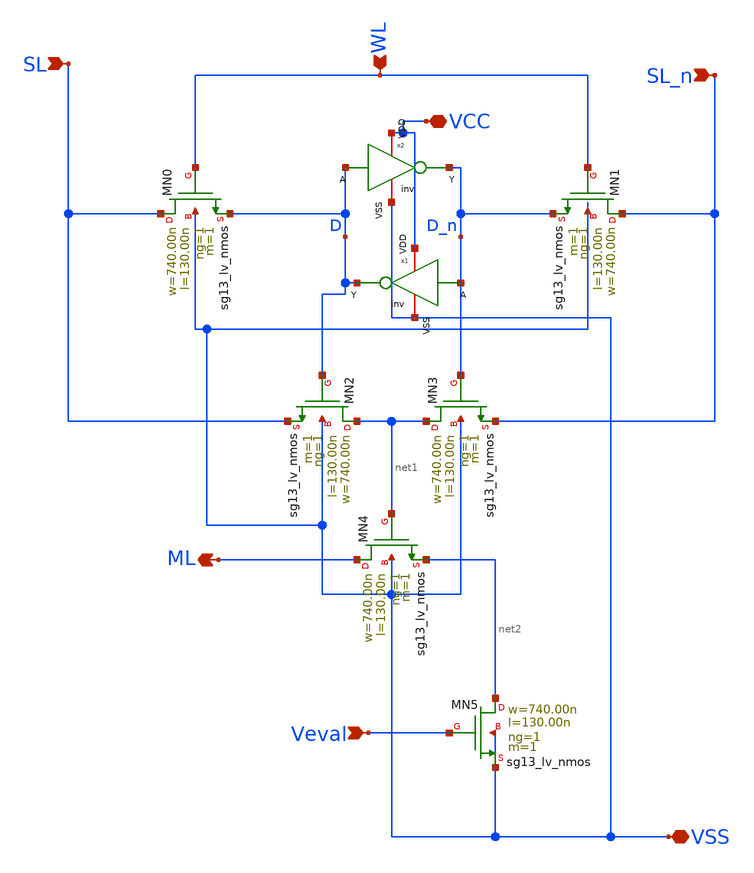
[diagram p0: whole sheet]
** sch_path: xschem/Cell.sch
**.subckt Cell SL SL_n Veval ML WL VSS VCC
*.ipin SL
*.ipin SL_n
*.ipin Veval
*.opin ML
*.ipin WL
*.iopin VSS
*.iopin VCC
XMN0 SL WL D VSS sg13_lv_nmos w=740.00n l=130.00n ng=1 m=1 mm_ok=1
XMN1 SL_n WL D_n VSS sg13_lv_nmos w=740.00n l=130.00n ng=1 m=1 mm_ok=1
XMN2 net1 D SL VSS sg13_lv_nmos w=740.00n l=130.00n ng=1 m=1 mm_ok=1
XMN3 net1 D_n SL_n VSS sg13_lv_nmos w=740.00n l=130.00n ng=1 m=1 mm_ok=1
XMN4 ML net1 net2 VSS sg13_lv_nmos w=740.00n l=130.00n ng=1 m=1 mm_ok=1
XMN5 net2 Veval VSS VSS sg13_lv_nmos w=740.00n l=130.00n ng=1 m=1 mm_ok=1
x1 VCC D D_n VSS inv
x2 VCC D_n D VSS inv
**.ends
.end
